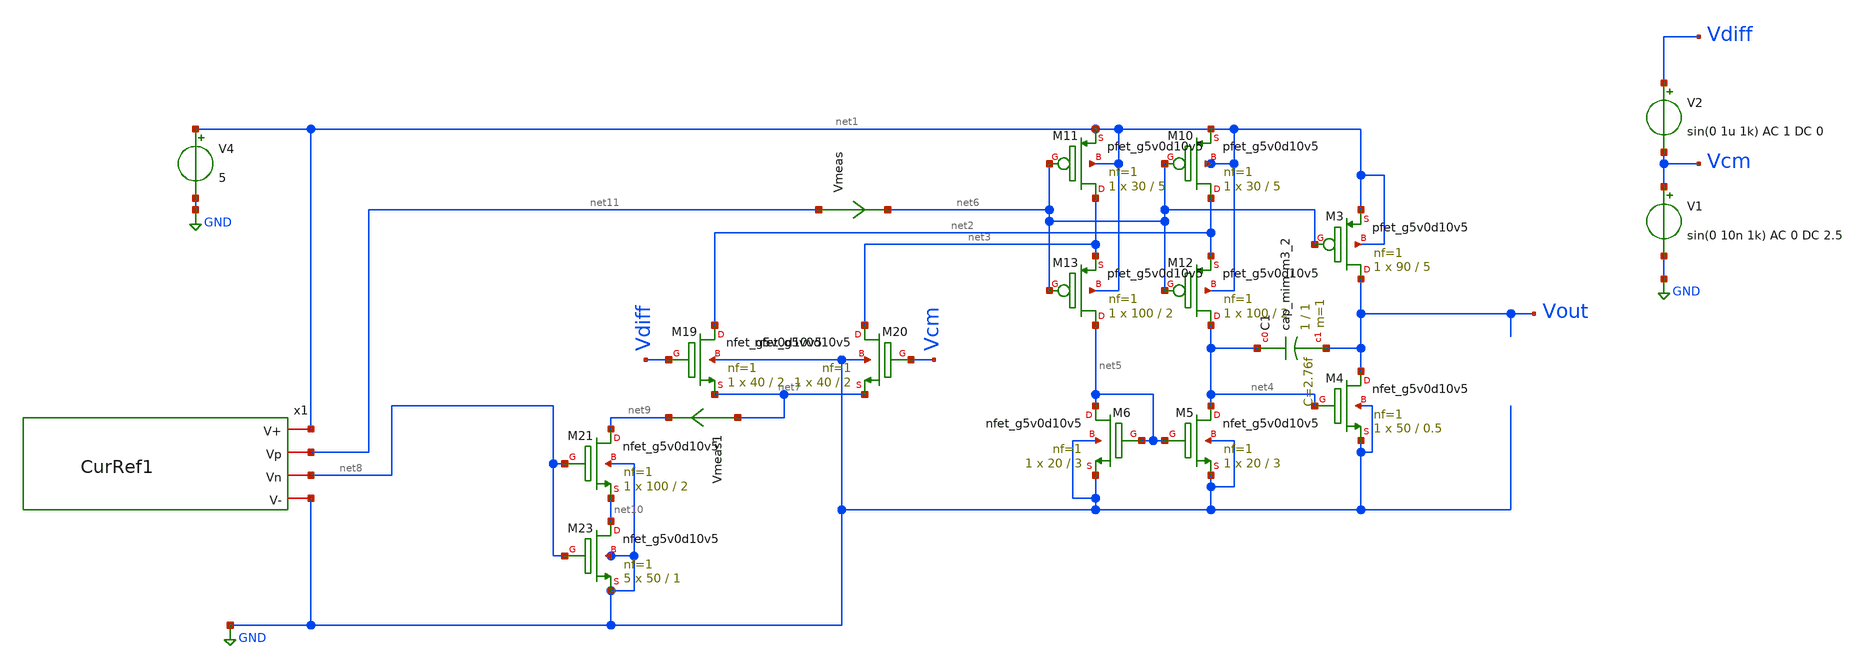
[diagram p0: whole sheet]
** sch_path: xschem/PrimalStructures/OpAmp2.sch
**.subckt OpAmp2
XM3 Vout net6 net1 net1 sky130_fd_pr__pfet_g5v0d10v5 L=5 W=90 nf=1 ad='int((nf+1)/2) * W/nf * 0.29' as='int((nf+2)/2) * W/nf * 0.29'
+ pd='2*int((nf+1)/2) * (W/nf + 0.29)' ps='2*int((nf+2)/2) * (W/nf + 0.29)' nrd='0.29 / W' nrs='0.29 / W'
+ sa=0 sb=0 sd=0 mult=1 m=1
XM4 Vout net4 GND GND sky130_fd_pr__nfet_g5v0d10v5 L=0.5 W=50 nf=1 ad='int((nf+1)/2) * W/nf * 0.29' as='int((nf+2)/2) * W/nf * 0.29'
+ pd='2*int((nf+1)/2) * (W/nf + 0.29)' ps='2*int((nf+2)/2) * (W/nf + 0.29)' nrd='0.29 / W' nrs='0.29 / W'
+ sa=0 sb=0 sd=0 mult=1 m=1
XM5 net4 net5 GND GND sky130_fd_pr__nfet_g5v0d10v5 L=3 W=20 nf=1 ad='int((nf+1)/2) * W/nf * 0.29' as='int((nf+2)/2) * W/nf * 0.29'
+ pd='2*int((nf+1)/2) * (W/nf + 0.29)' ps='2*int((nf+2)/2) * (W/nf + 0.29)' nrd='0.29 / W' nrs='0.29 / W'
+ sa=0 sb=0 sd=0 mult=1 m=1
XM6 net5 net5 GND GND sky130_fd_pr__nfet_g5v0d10v5 L=3 W=20 nf=1 ad='int((nf+1)/2) * W/nf * 0.29' as='int((nf+2)/2) * W/nf * 0.29'
+ pd='2*int((nf+1)/2) * (W/nf + 0.29)' ps='2*int((nf+2)/2) * (W/nf + 0.29)' nrd='0.29 / W' nrs='0.29 / W'
+ sa=0 sb=0 sd=0 mult=1 m=1
XM10 net2 net6 net1 net1 sky130_fd_pr__pfet_g5v0d10v5 L=5 W=30 nf=1 ad='int((nf+1)/2) * W/nf * 0.29'
+ as='int((nf+2)/2) * W/nf * 0.29' pd='2*int((nf+1)/2) * (W/nf + 0.29)' ps='2*int((nf+2)/2) * (W/nf + 0.29)'
+ nrd='0.29 / W' nrs='0.29 / W' sa=0 sb=0 sd=0 mult=1 m=1
XM11 net3 net6 net1 net1 sky130_fd_pr__pfet_g5v0d10v5 L=5 W=30 nf=1 ad='int((nf+1)/2) * W/nf * 0.29'
+ as='int((nf+2)/2) * W/nf * 0.29' pd='2*int((nf+1)/2) * (W/nf + 0.29)' ps='2*int((nf+2)/2) * (W/nf + 0.29)'
+ nrd='0.29 / W' nrs='0.29 / W' sa=0 sb=0 sd=0 mult=1 m=1
XM12 net4 net6 net2 net1 sky130_fd_pr__pfet_g5v0d10v5 L=2 W=100 nf=1 ad='int((nf+1)/2) * W/nf * 0.29'
+ as='int((nf+2)/2) * W/nf * 0.29' pd='2*int((nf+1)/2) * (W/nf + 0.29)' ps='2*int((nf+2)/2) * (W/nf + 0.29)'
+ nrd='0.29 / W' nrs='0.29 / W' sa=0 sb=0 sd=0 mult=1 m=1
XM13 net5 net6 net3 net1 sky130_fd_pr__pfet_g5v0d10v5 L=2 W=100 nf=1 ad='int((nf+1)/2) * W/nf * 0.29'
+ as='int((nf+2)/2) * W/nf * 0.29' pd='2*int((nf+1)/2) * (W/nf + 0.29)' ps='2*int((nf+2)/2) * (W/nf + 0.29)'
+ nrd='0.29 / W' nrs='0.29 / W' sa=0 sb=0 sd=0 mult=1 m=1
XM19 net2 Vdiff net7 GND sky130_fd_pr__nfet_g5v0d10v5 L=2 W=40 nf=1 ad='int((nf+1)/2) * W/nf * 0.29'
+ as='int((nf+2)/2) * W/nf * 0.29' pd='2*int((nf+1)/2) * (W/nf + 0.29)' ps='2*int((nf+2)/2) * (W/nf + 0.29)'
+ nrd='0.29 / W' nrs='0.29 / W' sa=0 sb=0 sd=0 mult=1 m=1
XM20 net3 Vcm net7 GND sky130_fd_pr__nfet_g5v0d10v5 L=2 W=40 nf=1 ad='int((nf+1)/2) * W/nf * 0.29' as='int((nf+2)/2) * W/nf * 0.29'
+ pd='2*int((nf+1)/2) * (W/nf + 0.29)' ps='2*int((nf+2)/2) * (W/nf + 0.29)' nrd='0.29 / W' nrs='0.29 / W'
+ sa=0 sb=0 sd=0 mult=1 m=1
XM21 net9 net8 net10 GND sky130_fd_pr__nfet_g5v0d10v5 L=2 W=100 nf=1 ad='int((nf+1)/2) * W/nf * 0.29'
+ as='int((nf+2)/2) * W/nf * 0.29' pd='2*int((nf+1)/2) * (W/nf + 0.29)' ps='2*int((nf+2)/2) * (W/nf + 0.29)'
+ nrd='0.29 / W' nrs='0.29 / W' sa=0 sb=0 sd=0 mult=1 m=1
XM23 net10 net8 GND GND sky130_fd_pr__nfet_g5v0d10v5 L=1 W=50 nf=1 ad='int((nf+1)/2) * W/nf * 0.29' as='int((nf+2)/2) * W/nf * 0.29'
+ pd='2*int((nf+1)/2) * (W/nf + 0.29)' ps='2*int((nf+2)/2) * (W/nf + 0.29)' nrd='0.29 / W' nrs='0.29 / W'
+ sa=0 sb=0 sd=0 mult=5 m=5
V4 net1 GND 5
Vmeas net11 net6 0
.save i(vmeas)
V1 Vcm GND sin(0 10n 1k) AC 0 DC 2.5
V2 Vdiff Vcm sin(0 1u 1k) AC 1 DC 0
x1 net1 net11 net8 GND CurRef1
Vmeas1 net7 net9 0
.save i(vmeas1)
XC1 net4 Vout sky130_fd_pr__cap_mim_m3_2 W=1 L=1 MF=1 m=1
**** begin user architecture code

** opencircuitdesign pdks install
.lib $::SKYWATER_MODELS/sky130.lib.spice tt



* this option enables mos model bin
* selection based on W/NF instead of W
.control
op
print all
save all
ac dec 100 1 1G
plot Vdb(Vout)
plot ph(Vout)
#plot -V(Out)
.endc


**** end user architecture code
**.ends

* expanding   symbol:  PrimalStructures/CurRef1.sym # of pins=4
** sym_path: xschem/PrimalStructures/CurRef1.sym
** sch_path: xschem/PrimalStructures/CurRef1.sch
.subckt CurRef1 V+ Vp Vn V-
*.iopin Vp
*.iopin V+
*.iopin V-
*.iopin Vn
XM1 net1 Vn net2 V- sky130_fd_pr__nfet_g5v0d10v5 L=2 W=20 nf=1 ad='int((nf+1)/2) * W/nf * 0.29' as='int((nf+2)/2) * W/nf * 0.29'
+ pd='2*int((nf+1)/2) * (W/nf + 0.29)' ps='2*int((nf+2)/2) * (W/nf + 0.29)' nrd='0.29 / W' nrs='0.29 / W'
+ sa=0 sb=0 sd=0 mult=1 m=1
XM2 net1 Vn net2 V- sky130_fd_pr__nfet_g5v0d10v5 L=2 W=20 nf=1 ad='int((nf+1)/2) * W/nf * 0.29' as='int((nf+2)/2) * W/nf * 0.29'
+ pd='2*int((nf+1)/2) * (W/nf + 0.29)' ps='2*int((nf+2)/2) * (W/nf + 0.29)' nrd='0.29 / W' nrs='0.29 / W'
+ sa=0 sb=0 sd=0 mult=1 m=1
XM3 net1 Vn net2 V- sky130_fd_pr__nfet_g5v0d10v5 L=2 W=20 nf=1 ad='int((nf+1)/2) * W/nf * 0.29' as='int((nf+2)/2) * W/nf * 0.29'
+ pd='2*int((nf+1)/2) * (W/nf + 0.29)' ps='2*int((nf+2)/2) * (W/nf + 0.29)' nrd='0.29 / W' nrs='0.29 / W'
+ sa=0 sb=0 sd=0 mult=1 m=1
XM4 net1 Vn net2 V- sky130_fd_pr__nfet_g5v0d10v5 L=2 W=20 nf=1 ad='int((nf+1)/2) * W/nf * 0.29' as='int((nf+2)/2) * W/nf * 0.29'
+ pd='2*int((nf+1)/2) * (W/nf + 0.29)' ps='2*int((nf+2)/2) * (W/nf + 0.29)' nrd='0.29 / W' nrs='0.29 / W'
+ sa=0 sb=0 sd=0 mult=1 m=1
XM5 net1 Vn net2 V- sky130_fd_pr__nfet_g5v0d10v5 L=2 W=20 nf=1 ad='int((nf+1)/2) * W/nf * 0.29' as='int((nf+2)/2) * W/nf * 0.29'
+ pd='2*int((nf+1)/2) * (W/nf + 0.29)' ps='2*int((nf+2)/2) * (W/nf + 0.29)' nrd='0.29 / W' nrs='0.29 / W'
+ sa=0 sb=0 sd=0 mult=1 m=1
XM6 net2 Vn V- V- sky130_fd_pr__nfet_g5v0d10v5 L=5 W=20 nf=1 ad='int((nf+1)/2) * W/nf * 0.29' as='int((nf+2)/2) * W/nf * 0.29'
+ pd='2*int((nf+1)/2) * (W/nf + 0.29)' ps='2*int((nf+2)/2) * (W/nf + 0.29)' nrd='0.29 / W' nrs='0.29 / W'
+ sa=0 sb=0 sd=0 mult=1 m=1
XR1 net3 Vn GND sky130_fd_pr__res_xhigh_po_1p41 L=85 mult=1 m=1
XM7 Vp Vp V+ V+ sky130_fd_pr__pfet_g5v0d10v5 L=2 W=20 nf=1 ad='int((nf+1)/2) * W/nf * 0.29' as='int((nf+2)/2) * W/nf * 0.29'
+ pd='2*int((nf+1)/2) * (W/nf + 0.29)' ps='2*int((nf+2)/2) * (W/nf + 0.29)' nrd='0.29 / W' nrs='0.29 / W'
+ sa=0 sb=0 sd=0 mult=1 m=1
XM8 Vp Vp V+ V+ sky130_fd_pr__pfet_g5v0d10v5 L=2 W=20 nf=1 ad='int((nf+1)/2) * W/nf * 0.29' as='int((nf+2)/2) * W/nf * 0.29'
+ pd='2*int((nf+1)/2) * (W/nf + 0.29)' ps='2*int((nf+2)/2) * (W/nf + 0.29)' nrd='0.29 / W' nrs='0.29 / W'
+ sa=0 sb=0 sd=0 mult=1 m=1
XM9 Vp Vp V+ V+ sky130_fd_pr__pfet_g5v0d10v5 L=2 W=20 nf=1 ad='int((nf+1)/2) * W/nf * 0.29' as='int((nf+2)/2) * W/nf * 0.29'
+ pd='2*int((nf+1)/2) * (W/nf + 0.29)' ps='2*int((nf+2)/2) * (W/nf + 0.29)' nrd='0.29 / W' nrs='0.29 / W'
+ sa=0 sb=0 sd=0 mult=1 m=1
XM10 Vp Vp V+ V+ sky130_fd_pr__pfet_g5v0d10v5 L=2 W=20 nf=1 ad='int((nf+1)/2) * W/nf * 0.29' as='int((nf+2)/2) * W/nf * 0.29'
+ pd='2*int((nf+1)/2) * (W/nf + 0.29)' ps='2*int((nf+2)/2) * (W/nf + 0.29)' nrd='0.29 / W' nrs='0.29 / W'
+ sa=0 sb=0 sd=0 mult=1 m=1
XM11 Vp Vp V+ V+ sky130_fd_pr__pfet_g5v0d10v5 L=2 W=20 nf=1 ad='int((nf+1)/2) * W/nf * 0.29' as='int((nf+2)/2) * W/nf * 0.29'
+ pd='2*int((nf+1)/2) * (W/nf + 0.29)' ps='2*int((nf+2)/2) * (W/nf + 0.29)' nrd='0.29 / W' nrs='0.29 / W'
+ sa=0 sb=0 sd=0 mult=1 m=1
XM12 V+ Vp V+ V+ sky130_fd_pr__pfet_g5v0d10v5 L=5 W=30 nf=1 ad='int((nf+1)/2) * W/nf * 0.29' as='int((nf+2)/2) * W/nf * 0.29'
+ pd='2*int((nf+1)/2) * (W/nf + 0.29)' ps='2*int((nf+2)/2) * (W/nf + 0.29)' nrd='0.29 / W' nrs='0.29 / W'
+ sa=0 sb=0 sd=0 mult=1 m=1
Vmeas Vp net3 0
.save i(vmeas)
.ends

.GLOBAL GND
.end
